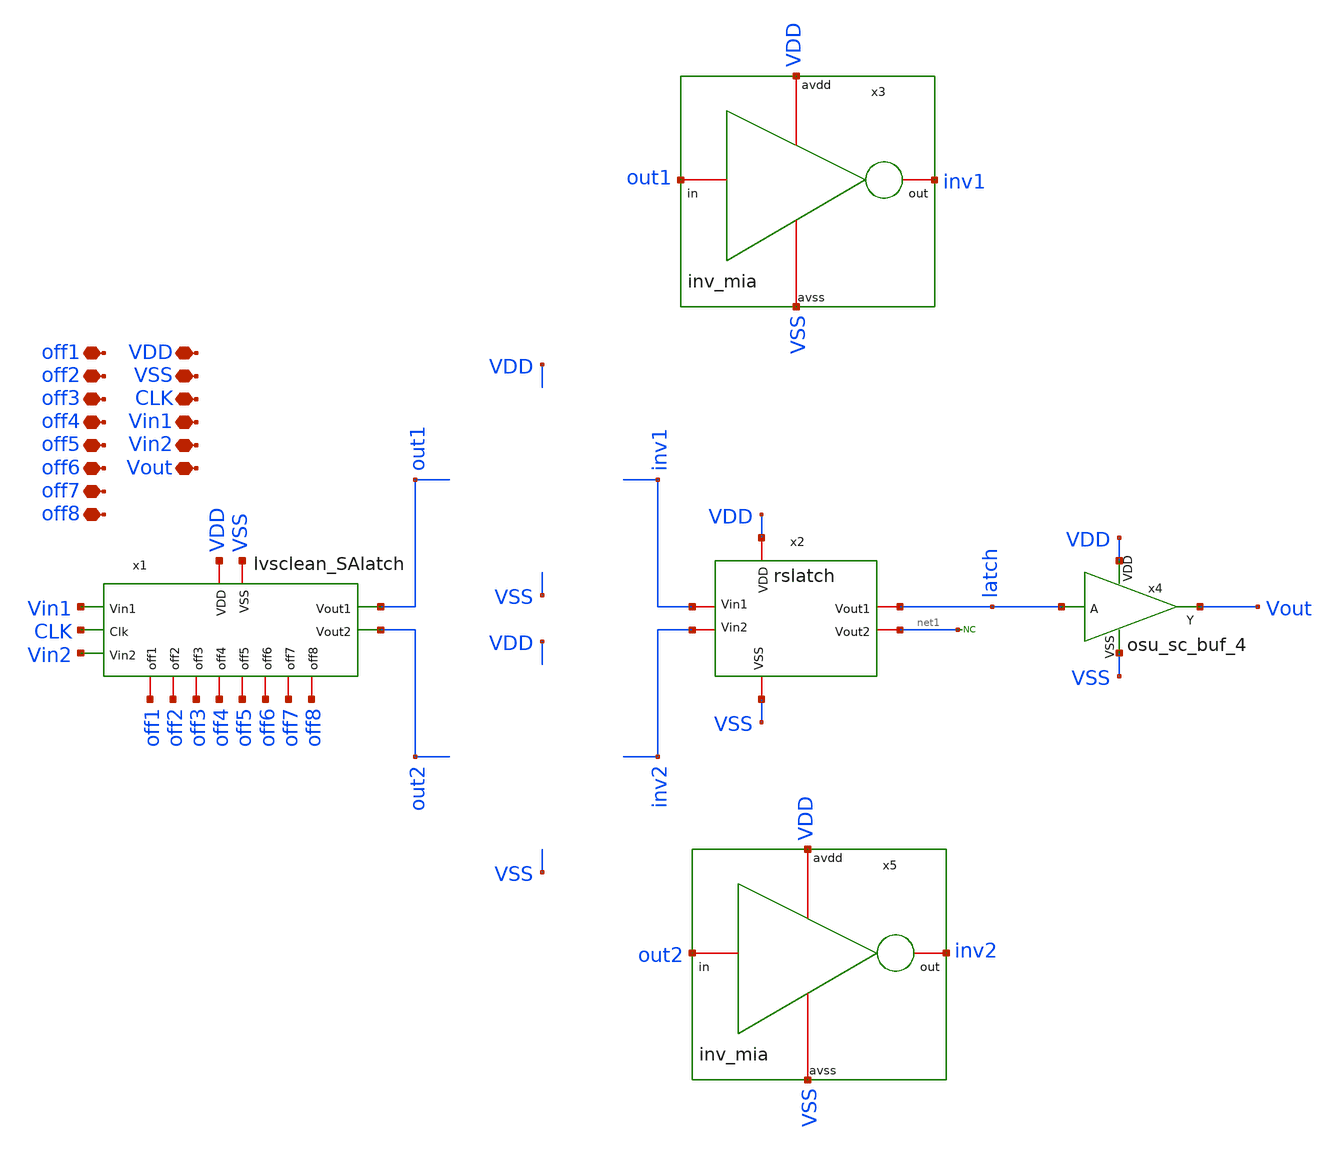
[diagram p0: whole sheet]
** sch_path: designs/comparator/final_magic/fullcomp/full_comparator.sch
**.subckt full_comparator VDD VSS CLK Vin1 Vin2 Vout off1 off2 off3 off4 off5 off6 off7 off8
*.iopin VDD
*.iopin VSS
*.iopin CLK
*.iopin Vin1
*.iopin Vin2
*.iopin Vout
*.iopin off1
*.iopin off2
*.iopin off3
*.iopin off4
*.iopin off5
*.iopin off6
*.iopin off7
*.iopin off8
* noconn #net1
x1 CLK Vin1 Vin2 VDD VSS out1 out2 off3 off2 off1 off8 off7 off6 off4 off5 lvsclean_SAlatch
x2 VDD latch net1 inv1 inv2 VSS rslatch
x4 VDD latch Vout VSS osu_sc_buf_4
x3 VDD out1 inv1 VSS inv_mia
x5 VDD out2 inv2 VSS inv_mia
**.ends
.end
